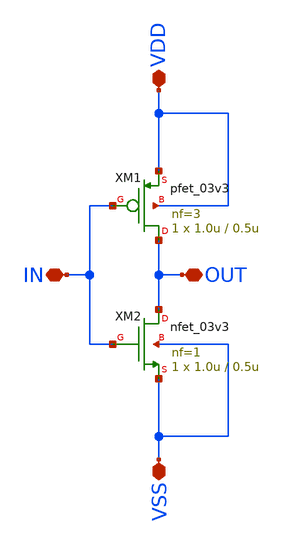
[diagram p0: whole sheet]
** sch_path: designs/libs/xp_core_analog/inv1u05u_cap/inv1u05u_cap.sch
**.subckt inv1u05u_cap IN OUT VSS VDD
*.iopin IN
*.iopin OUT
*.iopin VSS
*.iopin VDD
XM1 OUT IN VDD VDD pfet_03v3 L=0.5u W=1.0u nf=3 ad='int((nf+1)/2) * W/nf * 0.18u' as='int((nf+2)/2) * W/nf * 0.18u'
+ pd='2*int((nf+1)/2) * (W/nf + 0.18u)' ps='2*int((nf+2)/2) * (W/nf + 0.18u)' nrd='0.18u / W' nrs='0.18u / W'
+ sa=0 sb=0 sd=0 m=1
XM2 OUT IN VSS VSS nfet_03v3 L=0.5u W=1.0u nf=1 ad='int((nf+1)/2) * W/nf * 0.18u' as='int((nf+2)/2) * W/nf * 0.18u'
+ pd='2*int((nf+1)/2) * (W/nf + 0.18u)' ps='2*int((nf+2)/2) * (W/nf + 0.18u)' nrd='0.18u / W' nrs='0.18u / W'
+ sa=0 sb=0 sd=0 m=1
**.ends
.end
